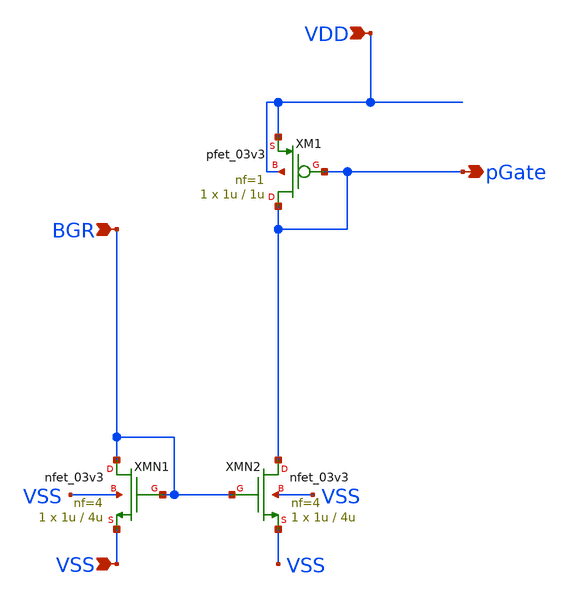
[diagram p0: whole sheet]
** sch_path: DAC/xschem/dac_global_current_mirror.sch
**.subckt dac_global_current_mirror BGR VDD pGate VSS
*.ipin BGR
*.ipin VDD
*.opin pGate
*.ipin VSS
XM1 pGate pGate VDD VDD pfet_03v3 L=1u W=1u nf=1 ad='int((nf+1)/2) * W/nf * 0.18u' as='int((nf+2)/2) * W/nf * 0.18u'
+ pd='2*int((nf+1)/2) * (W/nf + 0.18u)' ps='2*int((nf+2)/2) * (W/nf + 0.18u)' nrd='0.18u / W' nrs='0.18u / W'
+ sa=0 sb=0 sd=0 m=1
XMN1 BGR BGR VSS VSS nfet_03v3 L=4u W=1u nf=4 ad='int((nf+1)/2) * W/nf * 0.18u' as='int((nf+2)/2) * W/nf * 0.18u'
+ pd='2*int((nf+1)/2) * (W/nf + 0.18u)' ps='2*int((nf+2)/2) * (W/nf + 0.18u)' nrd='0.18u / W' nrs='0.18u / W'
+ sa=0 sb=0 sd=0 m=1
XMN2 pGate BGR VSS VSS nfet_03v3 L=4u W=1u nf=4 ad='int((nf+1)/2) * W/nf * 0.18u' as='int((nf+2)/2) * W/nf * 0.18u'
+ pd='2*int((nf+1)/2) * (W/nf + 0.18u)' ps='2*int((nf+2)/2) * (W/nf + 0.18u)' nrd='0.18u / W' nrs='0.18u / W'
+ sa=0 sb=0 sd=0 m=1
**.ends
.end
